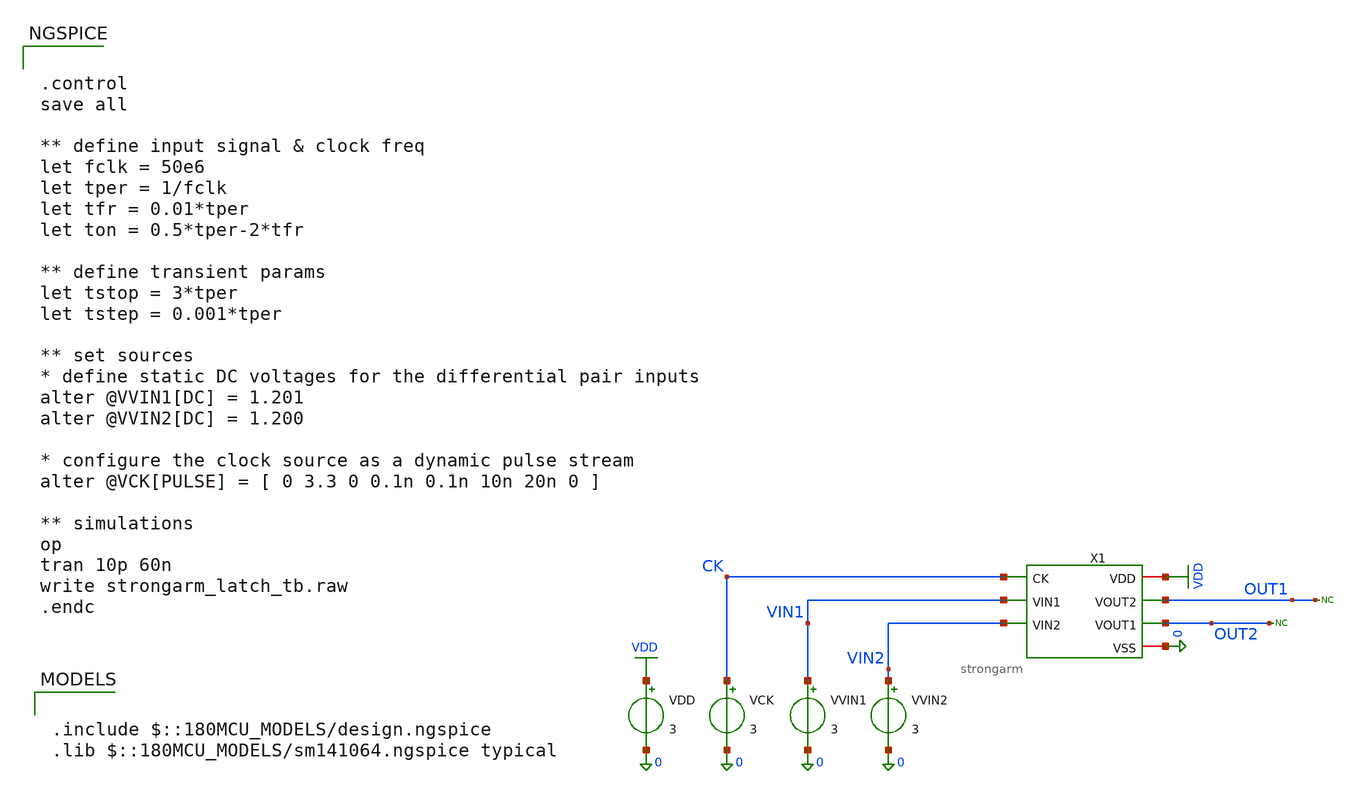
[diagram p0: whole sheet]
** sch_path: comparator/schematic/strongarm_tb.sch
**.subckt strongarm_tb
X1 VDD CK OUT1 OUT2 VIN1 VIN2 0 strongarm
VVIN2 VIN2 0 3
VVIN1 VIN1 0 3
VDD VDD 0 3
VCK CK 0 3
* noconn OUT2
* noconn OUT1
**** begin user architecture code

.include $::180MCU_MODELS/design.ngspice
.lib $::180MCU_MODELS/sm141064.ngspice typical



.control
save all

** define input signal & clock freq
let fclk = 50e6
let tper = 1/fclk
let tfr = 0.01*tper
let ton = 0.5*tper-2*tfr

** define transient params
let tstop = 3*tper
let tstep = 0.001*tper

** set sources
* define static DC voltages for the differential pair inputs
alter @VVIN1[DC] = 1.201
alter @VVIN2[DC] = 1.200

* configure the clock source as a dynamic pulse stream
alter @VCK[PULSE] = [ 0 3.3 0 0.1n 0.1n 10n 20n 0 ]

** simulations
op
tran 10p 60n
write strongarm_latch_tb.raw
.endc


**** end user architecture code
**.ends

* expanding   symbol:  comparator/schematic/strongarm.sym # of pins=7
** sym_path: comparator/schematic/strongarm.sym
** sch_path: comparator/schematic/strongarm.sch
.subckt strongarm VDD CK VOUT2 VOUT1 VIN1 VIN2 VSS
*.opin VOUT1
*.opin VOUT2
*.ipin VIN1
*.ipin VIN2
*.ipin CK
*.iopin VDD
*.iopin VSS
XM1 VOUT2 VOUT1 net1 net1 nfet_03v3 L=0.28u W=0.22u nf=1 ad='int((nf+1)/2) * W/nf * 0.18u' as='int((nf+2)/2) * W/nf * 0.18u'
+ pd='2*int((nf+1)/2) * (W/nf + 0.18u)' ps='2*int((nf+2)/2) * (W/nf + 0.18u)' nrd='0.18u / W' nrs='0.18u / W'
+ sa=0 sb=0 sd=0 m=1
XM2 VOUT1 VOUT2 VDD VDD pfet_03v3 L=0.28u W=0.22u nf=1 ad='int((nf+1)/2) * W/nf * 0.18u' as='int((nf+2)/2) * W/nf * 0.18u'
+ pd='2*int((nf+1)/2) * (W/nf + 0.18u)' ps='2*int((nf+2)/2) * (W/nf + 0.18u)' nrd='0.18u / W' nrs='0.18u / W'
+ sa=0 sb=0 sd=0 m=1
XM3 VOUT1 CK VDD VDD pfet_03v3 L=0.28u W=0.22u nf=1 ad='int((nf+1)/2) * W/nf * 0.18u' as='int((nf+2)/2) * W/nf * 0.18u'
+ pd='2*int((nf+1)/2) * (W/nf + 0.18u)' ps='2*int((nf+2)/2) * (W/nf + 0.18u)' nrd='0.18u / W' nrs='0.18u / W'
+ sa=0 sb=0 sd=0 m=1
XM4 net3 CK VDD VDD pfet_03v3 L=0.28u W=0.22u nf=1 ad='int((nf+1)/2) * W/nf * 0.18u' as='int((nf+2)/2) * W/nf * 0.18u'
+ pd='2*int((nf+1)/2) * (W/nf + 0.18u)' ps='2*int((nf+2)/2) * (W/nf + 0.18u)' nrd='0.18u / W' nrs='0.18u / W'
+ sa=0 sb=0 sd=0 m=1
XM5 net1 CK VDD VDD pfet_03v3 L=0.28u W=0.22u nf=1 ad='int((nf+1)/2) * W/nf * 0.18u' as='int((nf+2)/2) * W/nf * 0.18u'
+ pd='2*int((nf+1)/2) * (W/nf + 0.18u)' ps='2*int((nf+2)/2) * (W/nf + 0.18u)' nrd='0.18u / W' nrs='0.18u / W'
+ sa=0 sb=0 sd=0 m=1
XM6 VOUT2 CK VDD VDD pfet_03v3 L=0.28u W=0.22u nf=1 ad='int((nf+1)/2) * W/nf * 0.18u' as='int((nf+2)/2) * W/nf * 0.18u'
+ pd='2*int((nf+1)/2) * (W/nf + 0.18u)' ps='2*int((nf+2)/2) * (W/nf + 0.18u)' nrd='0.18u / W' nrs='0.18u / W'
+ sa=0 sb=0 sd=0 m=1
XM7 VOUT2 VOUT1 VDD VDD pfet_03v3 L=0.28u W=0.22u nf=1 ad='int((nf+1)/2) * W/nf * 0.18u' as='int((nf+2)/2) * W/nf * 0.18u'
+ pd='2*int((nf+1)/2) * (W/nf + 0.18u)' ps='2*int((nf+2)/2) * (W/nf + 0.18u)' nrd='0.18u / W' nrs='0.18u / W'
+ sa=0 sb=0 sd=0 m=1
XM8 net1 VIN2 net2 net2 nfet_03v3 L=0.28u W=0.22u nf=1 ad='int((nf+1)/2) * W/nf * 0.18u' as='int((nf+2)/2) * W/nf * 0.18u'
+ pd='2*int((nf+1)/2) * (W/nf + 0.18u)' ps='2*int((nf+2)/2) * (W/nf + 0.18u)' nrd='0.18u / W' nrs='0.18u / W'
+ sa=0 sb=0 sd=0 m=1
XM9 VOUT1 VOUT2 net3 net3 nfet_03v3 L=0.28u W=0.22u nf=1 ad='int((nf+1)/2) * W/nf * 0.18u' as='int((nf+2)/2) * W/nf * 0.18u'
+ pd='2*int((nf+1)/2) * (W/nf + 0.18u)' ps='2*int((nf+2)/2) * (W/nf + 0.18u)' nrd='0.18u / W' nrs='0.18u / W'
+ sa=0 sb=0 sd=0 m=1
XM10 net3 VIN1 net2 net2 nfet_03v3 L=0.28u W=0.22u nf=1 ad='int((nf+1)/2) * W/nf * 0.18u' as='int((nf+2)/2) * W/nf * 0.18u'
+ pd='2*int((nf+1)/2) * (W/nf + 0.18u)' ps='2*int((nf+2)/2) * (W/nf + 0.18u)' nrd='0.18u / W' nrs='0.18u / W'
+ sa=0 sb=0 sd=0 m=1
XM11 net2 CK VSS net2 nfet_03v3 L=0.28u W=0.22u nf=1 ad='int((nf+1)/2) * W/nf * 0.18u' as='int((nf+2)/2) * W/nf * 0.18u'
+ pd='2*int((nf+1)/2) * (W/nf + 0.18u)' ps='2*int((nf+2)/2) * (W/nf + 0.18u)' nrd='0.18u / W' nrs='0.18u / W'
+ sa=0 sb=0 sd=0 m=1
.ends

.GLOBAL VDD
.end
